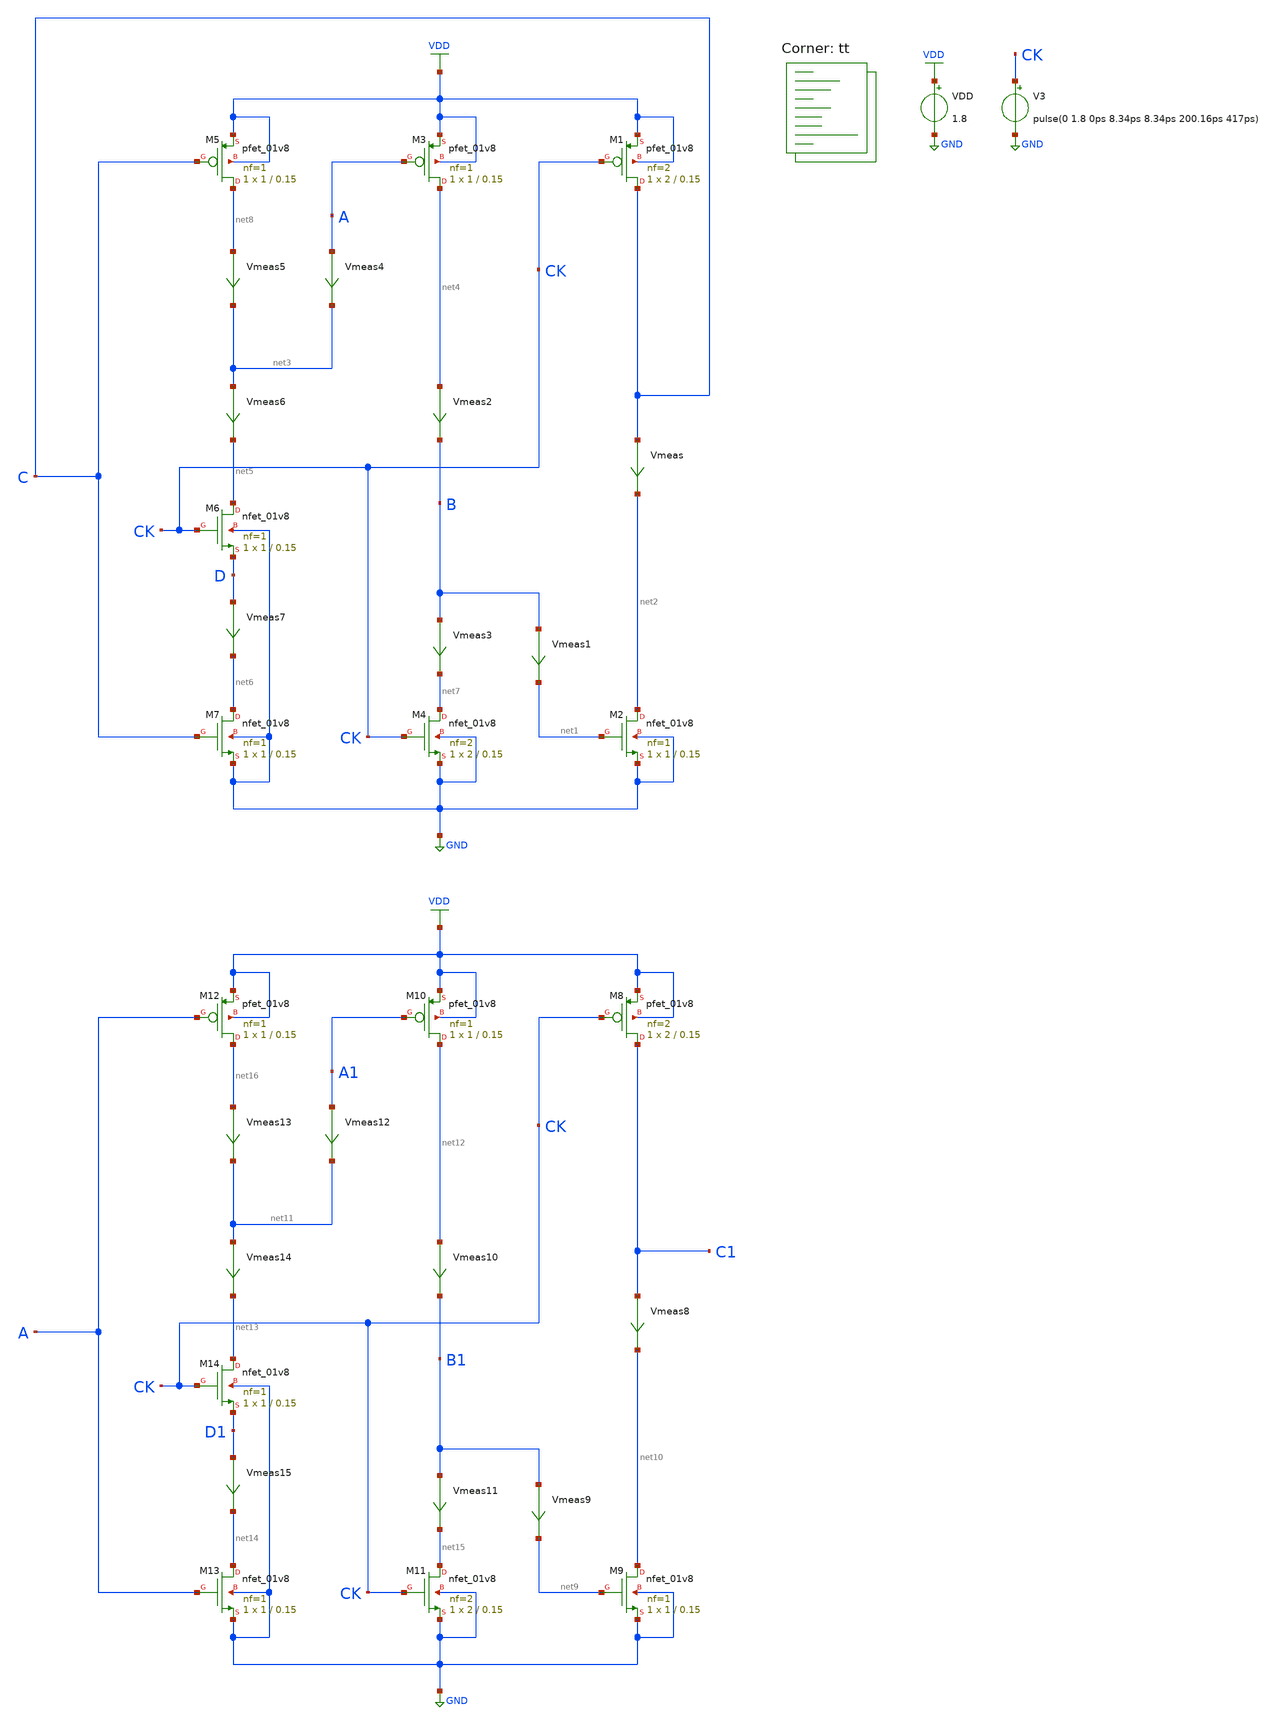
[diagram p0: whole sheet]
** sch_path: projects/pll/divider/xschem_ngspice/tb_TSPC_FF_ratioed_divide3.sch
**.subckt tb_TSPC_FF_ratioed_divide3
VDD VDD GND 1.8
V3 CK GND pulse(0 1.8 0ps 8.34ps 8.34ps 200.16ps 417ps)
XM1 C CK VDD VDD sky130_fd_pr__pfet_01v8 L=0.15 W=2 nf=2 ad='int((nf+1)/2) * W/nf * 0.29' as='int((nf+2)/2) * W/nf * 0.29'
+ pd='2*int((nf+1)/2) * (W/nf + 0.29)' ps='2*int((nf+2)/2) * (W/nf + 0.29)' nrd='0.29 / W' nrs='0.29 / W'
+ sa=0 sb=0 sd=0 mult=1 m=1
Vmeas C net2 0
.save i(vmeas)
XM2 net2 net1 GND GND sky130_fd_pr__nfet_01v8 L=0.15 W=1 nf=1 ad='int((nf+1)/2) * W/nf * 0.29' as='int((nf+2)/2) * W/nf * 0.29'
+ pd='2*int((nf+1)/2) * (W/nf + 0.29)' ps='2*int((nf+2)/2) * (W/nf + 0.29)' nrd='0.29 / W' nrs='0.29 / W'
+ sa=0 sb=0 sd=0 mult=1 m=1
XM3 net4 A VDD VDD sky130_fd_pr__pfet_01v8 L=0.15 W=1 nf=1 ad='int((nf+1)/2) * W/nf * 0.29' as='int((nf+2)/2) * W/nf * 0.29'
+ pd='2*int((nf+1)/2) * (W/nf + 0.29)' ps='2*int((nf+2)/2) * (W/nf + 0.29)' nrd='0.29 / W' nrs='0.29 / W'
+ sa=0 sb=0 sd=0 mult=1 m=1
XM4 net7 CK GND GND sky130_fd_pr__nfet_01v8 L=0.15 W=2 nf=2 ad='int((nf+1)/2) * W/nf * 0.29' as='int((nf+2)/2) * W/nf * 0.29'
+ pd='2*int((nf+1)/2) * (W/nf + 0.29)' ps='2*int((nf+2)/2) * (W/nf + 0.29)' nrd='0.29 / W' nrs='0.29 / W'
+ sa=0 sb=0 sd=0 mult=1 m=1
Vmeas1 B net1 0
.save i(vmeas1)
XM5 net8 C VDD VDD sky130_fd_pr__pfet_01v8 L=0.15 W=1 nf=1 ad='int((nf+1)/2) * W/nf * 0.29' as='int((nf+2)/2) * W/nf * 0.29'
+ pd='2*int((nf+1)/2) * (W/nf + 0.29)' ps='2*int((nf+2)/2) * (W/nf + 0.29)' nrd='0.29 / W' nrs='0.29 / W'
+ sa=0 sb=0 sd=0 mult=1 m=1
XM7 net6 C GND GND sky130_fd_pr__nfet_01v8 L=0.15 W=1 nf=1 ad='int((nf+1)/2) * W/nf * 0.29' as='int((nf+2)/2) * W/nf * 0.29'
+ pd='2*int((nf+1)/2) * (W/nf + 0.29)' ps='2*int((nf+2)/2) * (W/nf + 0.29)' nrd='0.29 / W' nrs='0.29 / W'
+ sa=0 sb=0 sd=0 mult=1 m=1
Vmeas2 net4 B 0
.save i(vmeas2)
XM6 net5 CK D GND sky130_fd_pr__nfet_01v8 L=0.15 W=1 nf=1 ad='int((nf+1)/2) * W/nf * 0.29' as='int((nf+2)/2) * W/nf * 0.29'
+ pd='2*int((nf+1)/2) * (W/nf + 0.29)' ps='2*int((nf+2)/2) * (W/nf + 0.29)' nrd='0.29 / W' nrs='0.29 / W'
+ sa=0 sb=0 sd=0 mult=1 m=1
Vmeas3 B net7 0
.save i(vmeas3)
Vmeas4 A net3 0
.save i(vmeas4)
Vmeas5 net8 net3 0
.save i(vmeas5)
Vmeas6 net3 net5 0
.save i(vmeas6)
Vmeas7 D net6 0
.save i(vmeas7)
XM8 C1 CK VDD VDD sky130_fd_pr__pfet_01v8 L=0.15 W=2 nf=2 ad='int((nf+1)/2) * W/nf * 0.29' as='int((nf+2)/2) * W/nf * 0.29'
+ pd='2*int((nf+1)/2) * (W/nf + 0.29)' ps='2*int((nf+2)/2) * (W/nf + 0.29)' nrd='0.29 / W' nrs='0.29 / W'
+ sa=0 sb=0 sd=0 mult=1 m=1
Vmeas8 C1 net10 0
.save i(vmeas8)
XM9 net10 net9 GND GND sky130_fd_pr__nfet_01v8 L=0.15 W=1 nf=1 ad='int((nf+1)/2) * W/nf * 0.29' as='int((nf+2)/2) * W/nf * 0.29'
+ pd='2*int((nf+1)/2) * (W/nf + 0.29)' ps='2*int((nf+2)/2) * (W/nf + 0.29)' nrd='0.29 / W' nrs='0.29 / W'
+ sa=0 sb=0 sd=0 mult=1 m=1
XM10 net12 A1 VDD VDD sky130_fd_pr__pfet_01v8 L=0.15 W=1 nf=1 ad='int((nf+1)/2) * W/nf * 0.29' as='int((nf+2)/2) * W/nf * 0.29'
+ pd='2*int((nf+1)/2) * (W/nf + 0.29)' ps='2*int((nf+2)/2) * (W/nf + 0.29)' nrd='0.29 / W' nrs='0.29 / W'
+ sa=0 sb=0 sd=0 mult=1 m=1
XM11 net15 CK GND GND sky130_fd_pr__nfet_01v8 L=0.15 W=2 nf=2 ad='int((nf+1)/2) * W/nf * 0.29' as='int((nf+2)/2) * W/nf * 0.29'
+ pd='2*int((nf+1)/2) * (W/nf + 0.29)' ps='2*int((nf+2)/2) * (W/nf + 0.29)' nrd='0.29 / W' nrs='0.29 / W'
+ sa=0 sb=0 sd=0 mult=1 m=1
Vmeas9 B1 net9 0
.save i(vmeas9)
XM12 net16 A VDD VDD sky130_fd_pr__pfet_01v8 L=0.15 W=1 nf=1 ad='int((nf+1)/2) * W/nf * 0.29' as='int((nf+2)/2) * W/nf * 0.29'
+ pd='2*int((nf+1)/2) * (W/nf + 0.29)' ps='2*int((nf+2)/2) * (W/nf + 0.29)' nrd='0.29 / W' nrs='0.29 / W'
+ sa=0 sb=0 sd=0 mult=1 m=1
XM13 net14 A GND GND sky130_fd_pr__nfet_01v8 L=0.15 W=1 nf=1 ad='int((nf+1)/2) * W/nf * 0.29' as='int((nf+2)/2) * W/nf * 0.29'
+ pd='2*int((nf+1)/2) * (W/nf + 0.29)' ps='2*int((nf+2)/2) * (W/nf + 0.29)' nrd='0.29 / W' nrs='0.29 / W'
+ sa=0 sb=0 sd=0 mult=1 m=1
Vmeas10 net12 B1 0
.save i(vmeas10)
XM14 net13 CK D1 GND sky130_fd_pr__nfet_01v8 L=0.15 W=1 nf=1 ad='int((nf+1)/2) * W/nf * 0.29' as='int((nf+2)/2) * W/nf * 0.29'
+ pd='2*int((nf+1)/2) * (W/nf + 0.29)' ps='2*int((nf+2)/2) * (W/nf + 0.29)' nrd='0.29 / W' nrs='0.29 / W'
+ sa=0 sb=0 sd=0 mult=1 m=1
Vmeas11 B1 net15 0
.save i(vmeas11)
Vmeas12 A1 net11 0
.save i(vmeas12)
Vmeas13 net16 net11 0
.save i(vmeas13)
Vmeas14 net11 net13 0
.save i(vmeas14)
Vmeas15 D1 net14 0
.save i(vmeas15)
**** begin user architecture code



.include /foss/pdks/sky130A/libs.ref/sky130_fd_sc_hd/spice/sky130_fd_sc_hd.spice

.option method=gear
.option wnflag=1
.option savecurrents

.save @m.xm1.msky130_fd_pr__pfet_01v8[gm] @m.xm2.msky130_fd_pr__nfet_01v8[gm] @m.xm3.msky130_fd_pr__pfet_01v8[gm] @m.xm4.msky130_fd_pr__nfet_01v8[gm] @m.xm5.msky130_fd_pr__pfet_01v8[gm] @m.xm6.msky130_fd_pr__nfet_01v8[gm] @m.xm7.msky130_fd_pr__nfet_01v8[gm] @m.xm8.msky130_fd_pr__pfet_01v8[gm] @m.xm9.msky130_fd_pr__nfet_01v8[gm] @m.xm10.msky130_fd_pr__nfet_01v8[gm]


.control

  save v(a) v(b) v(c) v(d) v(a1) v(b1) v(c1) v(d1) v(a2) v(b2) v(c2) v(d2) v(ck) v(vdd) v(gnd)
  * save all
  * tran 0.1n 1u
  tran 0.2p 10n

  remzerovec
  write tb_TSPC_FF_ratioed_divide3.raw
  set appendwrite

.endc



.lib $::SKYWATER_MODELS/sky130.lib.spice tt
**** end user architecture code
**.ends
.GLOBAL GND
.GLOBAL VDD
.end
